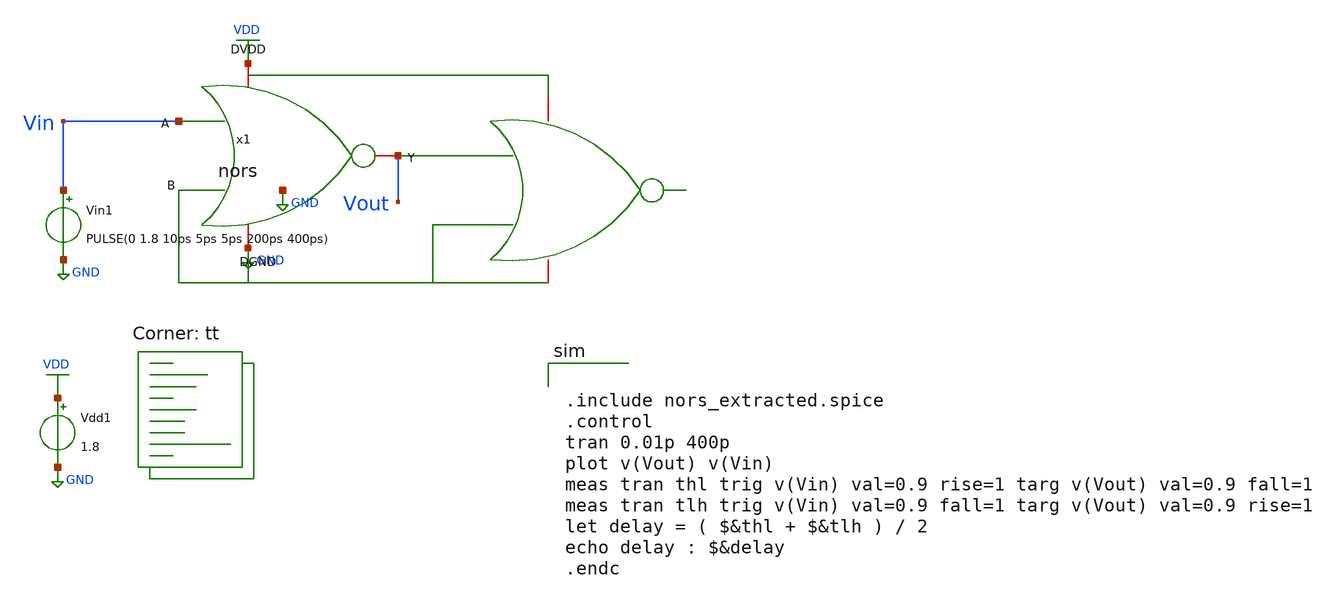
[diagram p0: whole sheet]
** sch_path: tutorial_7/tutorial_7v2.sch
**.subckt tutorial_7v2
Vin1 Vin GND PULSE(0 1.8 10ps 5ps 5ps 200ps 400ps)
Vdd1 VDD GND 1.8
x1 VDD Vout Vin GND nors
**** begin user architecture code
.lib $::SKYWATER_MODELS/sky130.lib.spice tt


.include nors_extracted.spice
.control
tran 0.01p 400p
plot v(Vout) v(Vin)
meas tran thl trig v(Vin) val=0.9 rise=1 targ v(Vout) val=0.9 fall=1
meas tran tlh trig v(Vin) val=0.9 fall=1 targ v(Vout) val=0.9 rise=1
let delay = ( $&thl + $&tlh ) / 2
echo delay : $&delay
.endc

**** end user architecture code
**.ends
.GLOBAL GND
.GLOBAL VDD
.end
